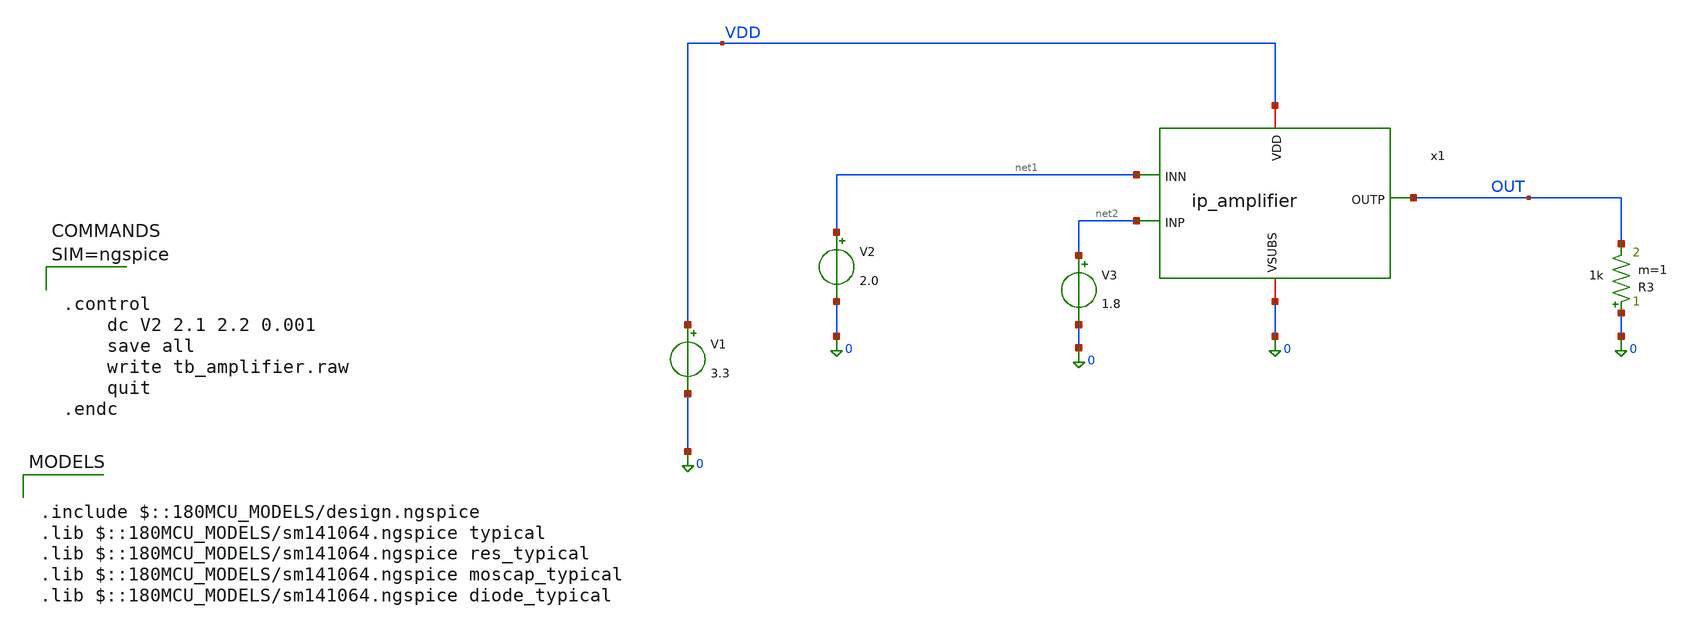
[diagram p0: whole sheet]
** sch_path: xschem/tb_amplifier.sch
**.subckt tb_amplifier
V1 VDD 0 3.3
x1 VDD OUT net2 net1 0 ip_amplifier
V2 net1 0 2.0
V3 net2 0 1.8
R3 0 OUT 1k m=1
**** begin user architecture code

.include $::180MCU_MODELS/design.ngspice
.lib $::180MCU_MODELS/sm141064.ngspice typical
.lib $::180MCU_MODELS/sm141064.ngspice res_typical
.lib $::180MCU_MODELS/sm141064.ngspice moscap_typical
.lib $::180MCU_MODELS/sm141064.ngspice diode_typical




.control
	dc V2 2.1 2.2 0.001
	save all
	write tb_amplifier.raw
	quit
.endc



**** end user architecture code
**.ends

* expanding   symbol:  ip_amplifier.sym # of pins=5
** sym_path: xschem/ip_amplifier.sym
** sch_path: xschem/ip_amplifier.sch
.subckt ip_amplifier VDD OUTP INP INN VSUBS
*.iopin VDD
*.iopin VSUBS
*.ipin INP
*.ipin INN
*.opin OUTP
XM1 net7 COM_P VDD VDD pfet_03v3 L=0.5u W=3.0u nf=1 ad='int((nf+1)/2) * W/nf * 0.18u' as='int((nf+2)/2) * W/nf * 0.18u'
+ pd='2*int((nf+1)/2) * (W/nf + 0.18u)' ps='2*int((nf+2)/2) * (W/nf + 0.18u)' nrd='0.18u / W' nrs='0.18u / W'
+ sa=0 sb=0 sd=0 m=1 par=1
XM2 net4 net2 net3 VSUBS nfet_03v3 L=2.0u W=10u nf=1 ad='int((nf+1)/2) * W/nf * 0.18u' as='int((nf+2)/2) * W/nf * 0.18u'
+ pd='2*int((nf+1)/2) * (W/nf + 0.18u)' ps='2*int((nf+2)/2) * (W/nf + 0.18u)' nrd='0.18u / W' nrs='0.18u / W'
+ sa=0 sb=0 sd=0 m=1 par=1
XM3 net3 net2 VSUBS VSUBS nfet_03v3 L=0.5u W=1.0u nf=1 ad='int((nf+1)/2) * W/nf * 0.18u' as='int((nf+2)/2) * W/nf * 0.18u'
+ pd='2*int((nf+1)/2) * (W/nf + 0.18u)' ps='2*int((nf+2)/2) * (W/nf + 0.18u)' nrd='0.18u / W' nrs='0.18u / W'
+ sa=0 sb=0 sd=0 m=1 par=1
XM4 net1 net2 VSUBS VSUBS nfet_03v3 L=0.5u W=1.0u nf=1 ad='int((nf+1)/2) * W/nf * 0.18u' as='int((nf+2)/2) * W/nf * 0.18u'
+ pd='2*int((nf+1)/2) * (W/nf + 0.18u)' ps='2*int((nf+2)/2) * (W/nf + 0.18u)' nrd='0.18u / W' nrs='0.18u / W'
+ sa=0 sb=0 sd=0 m=1 par=1
XM5 net5 COM_P VDD VDD pfet_03v3 L=0.5u W=3.0u nf=1 ad='int((nf+1)/2) * W/nf * 0.18u' as='int((nf+2)/2) * W/nf * 0.18u'
+ pd='2*int((nf+1)/2) * (W/nf + 0.18u)' ps='2*int((nf+2)/2) * (W/nf + 0.18u)' nrd='0.18u / W' nrs='0.18u / W'
+ sa=0 sb=0 sd=0 m=1 par=1
XM6 net6 COM_P net5 VDD pfet_03v3 L=2.0u W=10.0u nf=1 ad='int((nf+1)/2) * W/nf * 0.18u' as='int((nf+2)/2) * W/nf * 0.18u'
+ pd='2*int((nf+1)/2) * (W/nf + 0.18u)' ps='2*int((nf+2)/2) * (W/nf + 0.18u)' nrd='0.18u / W' nrs='0.18u / W'
+ sa=0 sb=0 sd=0 m=1 par=1
XM7 DIFF_L COM_P VDD VDD pfet_03v3 L=0.5u W=3.0u nf=1 ad='int((nf+1)/2) * W/nf * 0.18u' as='int((nf+2)/2) * W/nf * 0.18u'
+ pd='2*int((nf+1)/2) * (W/nf + 0.18u)' ps='2*int((nf+2)/2) * (W/nf + 0.18u)' nrd='0.18u / W' nrs='0.18u / W'
+ sa=0 sb=0 sd=0 m=1 par=1
XM9 DIFF_R COM_P VDD VDD pfet_03v3 L=0.5u W=3.0u nf=1 ad='int((nf+1)/2) * W/nf * 0.18u' as='int((nf+2)/2) * W/nf * 0.18u'
+ pd='2*int((nf+1)/2) * (W/nf + 0.18u)' ps='2*int((nf+2)/2) * (W/nf + 0.18u)' nrd='0.18u / W' nrs='0.18u / W'
+ sa=0 sb=0 sd=0 m=1 par=1
XM11 net12 INP net4 VSUBS nfet_03v3 L=0.3u W=4.0u nf=1 ad='int((nf+1)/2) * W/nf * 0.18u' as='int((nf+2)/2) * W/nf * 0.18u'
+ pd='2*int((nf+1)/2) * (W/nf + 0.18u)' ps='2*int((nf+2)/2) * (W/nf + 0.18u)' nrd='0.18u / W' nrs='0.18u / W'
+ sa=0 sb=0 sd=0 m=1 par=1
XM12 net13 INN net4 VSUBS nfet_03v3 L=0.3u W=4.0u nf=1 ad='int((nf+1)/2) * W/nf * 0.18u' as='int((nf+2)/2) * W/nf * 0.18u'
+ pd='2*int((nf+1)/2) * (W/nf + 0.18u)' ps='2*int((nf+2)/2) * (W/nf + 0.18u)' nrd='0.18u / W' nrs='0.18u / W'
+ sa=0 sb=0 sd=0 m=1 par=1
XM8 net10 COM_P DIFF_L VDD pfet_03v3 L=2.0u W=10.0u nf=1 ad='int((nf+1)/2) * W/nf * 0.18u' as='int((nf+2)/2) * W/nf * 0.18u'
+ pd='2*int((nf+1)/2) * (W/nf + 0.18u)' ps='2*int((nf+2)/2) * (W/nf + 0.18u)' nrd='0.18u / W' nrs='0.18u / W'
+ sa=0 sb=0 sd=0 m=1 par=1
XM10 net11 COM_P DIFF_R VDD pfet_03v3 L=2.0u W=10.0u nf=1 ad='int((nf+1)/2) * W/nf * 0.18u' as='int((nf+2)/2) * W/nf * 0.18u'
+ pd='2*int((nf+1)/2) * (W/nf + 0.18u)' ps='2*int((nf+2)/2) * (W/nf + 0.18u)' nrd='0.18u / W' nrs='0.18u / W'
+ sa=0 sb=0 sd=0 m=1 par=1
XM13 net9 net8 VSUBS VSUBS nfet_03v3 L=0.3u W=2.0u nf=1 ad='int((nf+1)/2) * W/nf * 0.18u' as='int((nf+2)/2) * W/nf * 0.18u'
+ pd='2*int((nf+1)/2) * (W/nf + 0.18u)' ps='2*int((nf+2)/2) * (W/nf + 0.18u)' nrd='0.18u / W' nrs='0.18u / W'
+ sa=0 sb=0 sd=0 m=1 par=1
XM14 net8 net8 VSUBS VSUBS nfet_03v3 L=0.3u W=2.0u nf=1 ad='int((nf+1)/2) * W/nf * 0.18u' as='int((nf+2)/2) * W/nf * 0.18u'
+ pd='2*int((nf+1)/2) * (W/nf + 0.18u)' ps='2*int((nf+2)/2) * (W/nf + 0.18u)' nrd='0.18u / W' nrs='0.18u / W'
+ sa=0 sb=0 sd=0 m=1 par=1
XM15 OUTP COM_P VDD VDD pfet_03v3 L=0.5u W=9u nf=1 ad='int((nf+1)/2) * W/nf * 0.18u' as='int((nf+2)/2) * W/nf * 0.18u'
+ pd='2*int((nf+1)/2) * (W/nf + 0.18u)' ps='2*int((nf+2)/2) * (W/nf + 0.18u)' nrd='0.18u / W' nrs='0.18u / W'
+ sa=0 sb=0 sd=0 m=1 par=1
XM16 OUTP net9 VSUBS VSUBS nfet_03v3 L=0.5u W=5.0u nf=1 ad='int((nf+1)/2) * W/nf * 0.18u' as='int((nf+2)/2) * W/nf * 0.18u'
+ pd='2*int((nf+1)/2) * (W/nf + 0.18u)' ps='2*int((nf+2)/2) * (W/nf + 0.18u)' nrd='0.18u / W' nrs='0.18u / W'
+ sa=0 sb=0 sd=0 m=1 par=1
R1 COM_P net14 130k m=1
Vmeas net14 VSUBS 0
Vmeas1 net6 net2 0
Vmeas2 net10 net8 0
Vmeas3 net11 net9 0
Vmeas4 DIFF_R net13 0
Vmeas5 DIFF_L net12 0
C1 OUTP net9 1p m=1
XM17 COM_P COM_P net7 VDD pfet_03v3 L=2.0u W=10.0u nf=1 ad='int((nf+1)/2) * W/nf * 0.18u' as='int((nf+2)/2) * W/nf * 0.18u'
+ pd='2*int((nf+1)/2) * (W/nf + 0.18u)' ps='2*int((nf+2)/2) * (W/nf + 0.18u)' nrd='0.18u / W' nrs='0.18u / W'
+ sa=0 sb=0 sd=0 m=1 par=1
XM18 net2 net2 net1 VSUBS nfet_03v3 L=2.0u W=10u nf=1 ad='int((nf+1)/2) * W/nf * 0.18u' as='int((nf+2)/2) * W/nf * 0.18u'
+ pd='2*int((nf+1)/2) * (W/nf + 0.18u)' ps='2*int((nf+2)/2) * (W/nf + 0.18u)' nrd='0.18u / W' nrs='0.18u / W'
+ sa=0 sb=0 sd=0 m=1 par=1
.ends

.end
